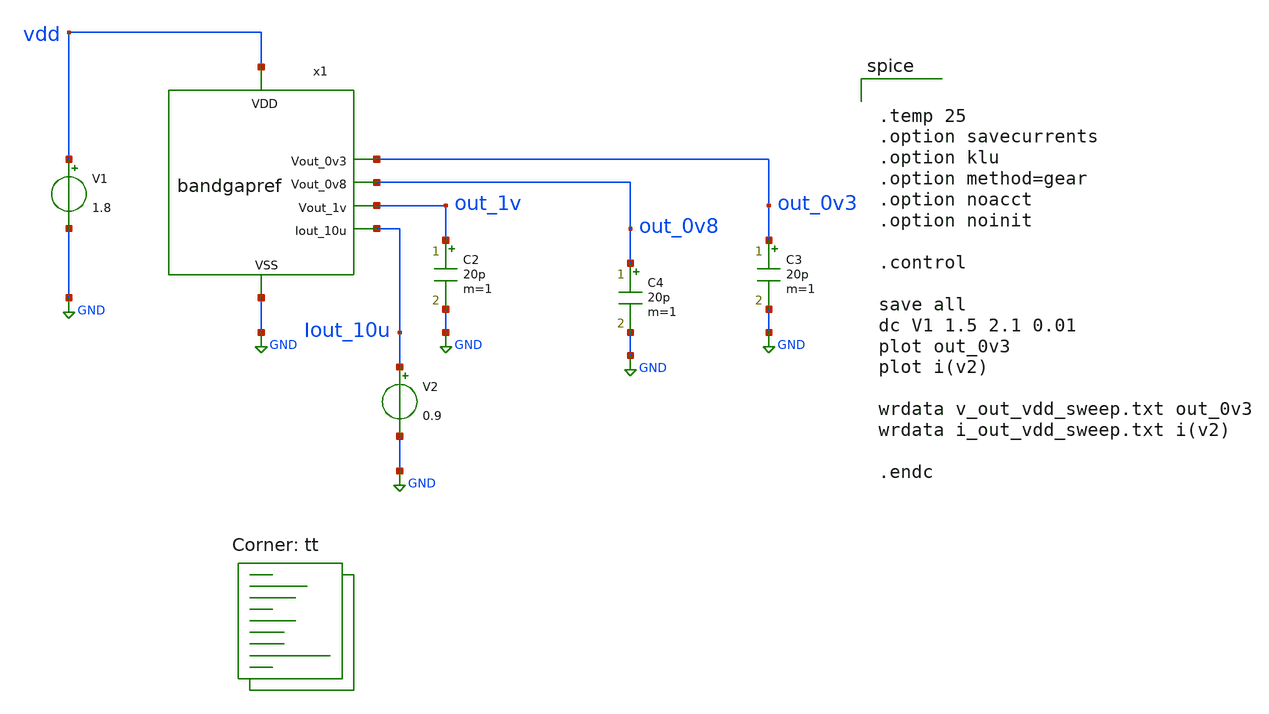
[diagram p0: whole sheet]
** sch_path: bandgapref_vdd_sweep_tb.sch
**.subckt bandgapref_vdd_sweep_tb
V1 vdd GND 1.8
.save i(v1)
x1 vdd out_0v3 GND out_1v out_0v8 Iout_10u bandgapref
C2 out_1v GND 20p m=1
C3 out_0v3 GND 20p m=1
C4 out_0v8 GND 20p m=1
V2 Iout_10u GND 0.9
.save i(v2)
**** begin user architecture code
.lib $::SKYWATER_MODELS/sky130.lib.spice tt


.temp 25
.option savecurrents
.option klu
.option method=gear
.option noacct
.option noinit

.control

save all
dc V1 1.5 2.1 0.01
plot out_0v3
plot i(v2)

wrdata v_out_vdd_sweep.txt out_0v3
wrdata i_out_vdd_sweep.txt i(v2)

.endc

**** end user architecture code
**.ends
.GLOBAL GND
.end
